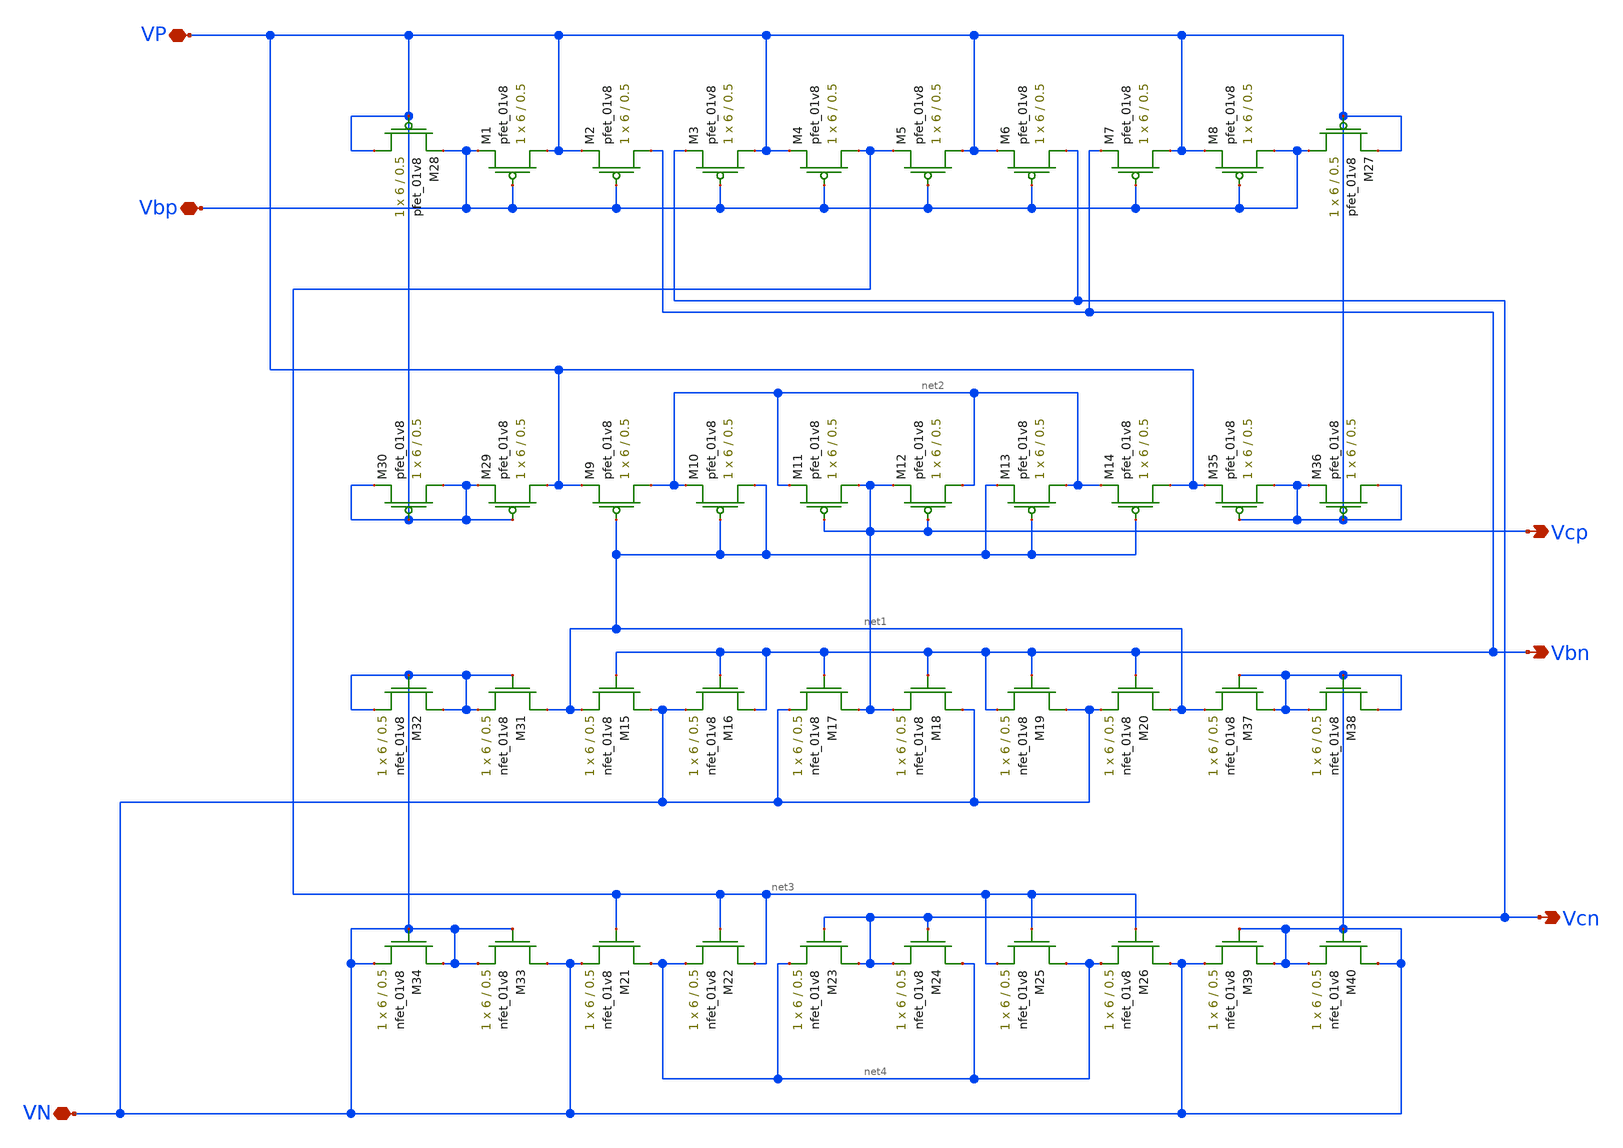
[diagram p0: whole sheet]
** sch_path: MP3/bias-lds.sch
**.subckt bias-lds VP VN Vbp Vcp VN Vbn Vcn
*.iopin VP
*.iopin VN
*.iopin Vbp
*.opin Vcp
*.iopin VN
*.opin Vbn
*.opin Vcn
XM1 VP Vbp Vbp VDD sky130_fd_pr__pfet_01v8 L=0.5 W=6 nf=1 ad='int((nf+1)/2) * W/nf * 0.29' as='int((nf+2)/2) * W/nf * 0.29'
+ pd='2*int((nf+1)/2) * (W/nf + 0.29)' ps='2*int((nf+2)/2) * (W/nf + 0.29)' nrd='0.29 / W' nrs='0.29 / W'
+ sa=0 sb=0 sd=0 mult=1 m=1
XM2 Vbn Vbp VP VDD sky130_fd_pr__pfet_01v8 L=0.5 W=6 nf=1 ad='int((nf+1)/2) * W/nf * 0.29' as='int((nf+2)/2) * W/nf * 0.29'
+ pd='2*int((nf+1)/2) * (W/nf + 0.29)' ps='2*int((nf+2)/2) * (W/nf + 0.29)' nrd='0.29 / W' nrs='0.29 / W'
+ sa=0 sb=0 sd=0 mult=1 m=1
XM3 VP Vbp Vcn VDD sky130_fd_pr__pfet_01v8 L=0.5 W=6 nf=1 ad='int((nf+1)/2) * W/nf * 0.29' as='int((nf+2)/2) * W/nf * 0.29'
+ pd='2*int((nf+1)/2) * (W/nf + 0.29)' ps='2*int((nf+2)/2) * (W/nf + 0.29)' nrd='0.29 / W' nrs='0.29 / W'
+ sa=0 sb=0 sd=0 mult=1 m=1
XM4 net3 Vbp VP VDD sky130_fd_pr__pfet_01v8 L=0.5 W=6 nf=1 ad='int((nf+1)/2) * W/nf * 0.29' as='int((nf+2)/2) * W/nf * 0.29'
+ pd='2*int((nf+1)/2) * (W/nf + 0.29)' ps='2*int((nf+2)/2) * (W/nf + 0.29)' nrd='0.29 / W' nrs='0.29 / W'
+ sa=0 sb=0 sd=0 mult=1 m=1
XM5 VP Vbp net3 VDD sky130_fd_pr__pfet_01v8 L=0.5 W=6 nf=1 ad='int((nf+1)/2) * W/nf * 0.29' as='int((nf+2)/2) * W/nf * 0.29'
+ pd='2*int((nf+1)/2) * (W/nf + 0.29)' ps='2*int((nf+2)/2) * (W/nf + 0.29)' nrd='0.29 / W' nrs='0.29 / W'
+ sa=0 sb=0 sd=0 mult=1 m=1
XM6 Vcn Vbp VP VDD sky130_fd_pr__pfet_01v8 L=0.5 W=6 nf=1 ad='int((nf+1)/2) * W/nf * 0.29' as='int((nf+2)/2) * W/nf * 0.29'
+ pd='2*int((nf+1)/2) * (W/nf + 0.29)' ps='2*int((nf+2)/2) * (W/nf + 0.29)' nrd='0.29 / W' nrs='0.29 / W'
+ sa=0 sb=0 sd=0 mult=1 m=1
XM7 VP Vbp Vbn VDD sky130_fd_pr__pfet_01v8 L=0.5 W=6 nf=1 ad='int((nf+1)/2) * W/nf * 0.29' as='int((nf+2)/2) * W/nf * 0.29'
+ pd='2*int((nf+1)/2) * (W/nf + 0.29)' ps='2*int((nf+2)/2) * (W/nf + 0.29)' nrd='0.29 / W' nrs='0.29 / W'
+ sa=0 sb=0 sd=0 mult=1 m=1
XM8 Vbp Vbp VP VDD sky130_fd_pr__pfet_01v8 L=0.5 W=6 nf=1 ad='int((nf+1)/2) * W/nf * 0.29' as='int((nf+2)/2) * W/nf * 0.29'
+ pd='2*int((nf+1)/2) * (W/nf + 0.29)' ps='2*int((nf+2)/2) * (W/nf + 0.29)' nrd='0.29 / W' nrs='0.29 / W'
+ sa=0 sb=0 sd=0 mult=1 m=1
XM9 net2 net1 VP VDD sky130_fd_pr__pfet_01v8 L=0.5 W=6 nf=1 ad='int((nf+1)/2) * W/nf * 0.29' as='int((nf+2)/2) * W/nf * 0.29'
+ pd='2*int((nf+1)/2) * (W/nf + 0.29)' ps='2*int((nf+2)/2) * (W/nf + 0.29)' nrd='0.29 / W' nrs='0.29 / W'
+ sa=0 sb=0 sd=0 mult=1 m=1
XM10 net1 net1 net2 VDD sky130_fd_pr__pfet_01v8 L=0.5 W=6 nf=1 ad='int((nf+1)/2) * W/nf * 0.29' as='int((nf+2)/2) * W/nf * 0.29'
+ pd='2*int((nf+1)/2) * (W/nf + 0.29)' ps='2*int((nf+2)/2) * (W/nf + 0.29)' nrd='0.29 / W' nrs='0.29 / W'
+ sa=0 sb=0 sd=0 mult=1 m=1
XM11 Vcp Vcp net2 VDD sky130_fd_pr__pfet_01v8 L=0.5 W=6 nf=1 ad='int((nf+1)/2) * W/nf * 0.29' as='int((nf+2)/2) * W/nf * 0.29'
+ pd='2*int((nf+1)/2) * (W/nf + 0.29)' ps='2*int((nf+2)/2) * (W/nf + 0.29)' nrd='0.29 / W' nrs='0.29 / W'
+ sa=0 sb=0 sd=0 mult=1 m=1
XM12 net2 Vcp Vcp VDD sky130_fd_pr__pfet_01v8 L=0.5 W=6 nf=1 ad='int((nf+1)/2) * W/nf * 0.29' as='int((nf+2)/2) * W/nf * 0.29'
+ pd='2*int((nf+1)/2) * (W/nf + 0.29)' ps='2*int((nf+2)/2) * (W/nf + 0.29)' nrd='0.29 / W' nrs='0.29 / W'
+ sa=0 sb=0 sd=0 mult=1 m=1
XM13 net2 net1 net1 VDD sky130_fd_pr__pfet_01v8 L=0.5 W=6 nf=1 ad='int((nf+1)/2) * W/nf * 0.29' as='int((nf+2)/2) * W/nf * 0.29'
+ pd='2*int((nf+1)/2) * (W/nf + 0.29)' ps='2*int((nf+2)/2) * (W/nf + 0.29)' nrd='0.29 / W' nrs='0.29 / W'
+ sa=0 sb=0 sd=0 mult=1 m=1
XM14 VP net1 net2 VDD sky130_fd_pr__pfet_01v8 L=0.5 W=6 nf=1 ad='int((nf+1)/2) * W/nf * 0.29' as='int((nf+2)/2) * W/nf * 0.29'
+ pd='2*int((nf+1)/2) * (W/nf + 0.29)' ps='2*int((nf+2)/2) * (W/nf + 0.29)' nrd='0.29 / W' nrs='0.29 / W'
+ sa=0 sb=0 sd=0 mult=1 m=1
XM15 VN Vbn net1 GND sky130_fd_pr__nfet_01v8 L=0.5 W=6 nf=1 ad='int((nf+1)/2) * W/nf * 0.29' as='int((nf+2)/2) * W/nf * 0.29'
+ pd='2*int((nf+1)/2) * (W/nf + 0.29)' ps='2*int((nf+2)/2) * (W/nf + 0.29)' nrd='0.29 / W' nrs='0.29 / W'
+ sa=0 sb=0 sd=0 mult=1 m=1
XM16 Vbn Vbn VN GND sky130_fd_pr__nfet_01v8 L=0.5 W=6 nf=1 ad='int((nf+1)/2) * W/nf * 0.29' as='int((nf+2)/2) * W/nf * 0.29'
+ pd='2*int((nf+1)/2) * (W/nf + 0.29)' ps='2*int((nf+2)/2) * (W/nf + 0.29)' nrd='0.29 / W' nrs='0.29 / W'
+ sa=0 sb=0 sd=0 mult=1 m=1
XM17 Vcp Vbn VN GND sky130_fd_pr__nfet_01v8 L=0.5 W=6 nf=1 ad='int((nf+1)/2) * W/nf * 0.29' as='int((nf+2)/2) * W/nf * 0.29'
+ pd='2*int((nf+1)/2) * (W/nf + 0.29)' ps='2*int((nf+2)/2) * (W/nf + 0.29)' nrd='0.29 / W' nrs='0.29 / W'
+ sa=0 sb=0 sd=0 mult=1 m=1
XM18 VN Vbn Vcp GND sky130_fd_pr__nfet_01v8 L=0.5 W=6 nf=1 ad='int((nf+1)/2) * W/nf * 0.29' as='int((nf+2)/2) * W/nf * 0.29'
+ pd='2*int((nf+1)/2) * (W/nf + 0.29)' ps='2*int((nf+2)/2) * (W/nf + 0.29)' nrd='0.29 / W' nrs='0.29 / W'
+ sa=0 sb=0 sd=0 mult=1 m=1
XM19 VN Vbn Vbn GND sky130_fd_pr__nfet_01v8 L=0.5 W=6 nf=1 ad='int((nf+1)/2) * W/nf * 0.29' as='int((nf+2)/2) * W/nf * 0.29'
+ pd='2*int((nf+1)/2) * (W/nf + 0.29)' ps='2*int((nf+2)/2) * (W/nf + 0.29)' nrd='0.29 / W' nrs='0.29 / W'
+ sa=0 sb=0 sd=0 mult=1 m=1
XM20 net1 Vbn VN GND sky130_fd_pr__nfet_01v8 L=0.5 W=6 nf=1 ad='int((nf+1)/2) * W/nf * 0.29' as='int((nf+2)/2) * W/nf * 0.29'
+ pd='2*int((nf+1)/2) * (W/nf + 0.29)' ps='2*int((nf+2)/2) * (W/nf + 0.29)' nrd='0.29 / W' nrs='0.29 / W'
+ sa=0 sb=0 sd=0 mult=1 m=1
XM21 net4 net3 VN GND sky130_fd_pr__nfet_01v8 L=0.5 W=6 nf=1 ad='int((nf+1)/2) * W/nf * 0.29' as='int((nf+2)/2) * W/nf * 0.29'
+ pd='2*int((nf+1)/2) * (W/nf + 0.29)' ps='2*int((nf+2)/2) * (W/nf + 0.29)' nrd='0.29 / W' nrs='0.29 / W'
+ sa=0 sb=0 sd=0 mult=1 m=1
XM22 net3 net3 net4 GND sky130_fd_pr__nfet_01v8 L=0.5 W=6 nf=1 ad='int((nf+1)/2) * W/nf * 0.29' as='int((nf+2)/2) * W/nf * 0.29'
+ pd='2*int((nf+1)/2) * (W/nf + 0.29)' ps='2*int((nf+2)/2) * (W/nf + 0.29)' nrd='0.29 / W' nrs='0.29 / W'
+ sa=0 sb=0 sd=0 mult=1 m=1
XM23 Vcn Vcn net4 GND sky130_fd_pr__nfet_01v8 L=0.5 W=6 nf=1 ad='int((nf+1)/2) * W/nf * 0.29' as='int((nf+2)/2) * W/nf * 0.29'
+ pd='2*int((nf+1)/2) * (W/nf + 0.29)' ps='2*int((nf+2)/2) * (W/nf + 0.29)' nrd='0.29 / W' nrs='0.29 / W'
+ sa=0 sb=0 sd=0 mult=1 m=1
XM24 net4 Vcn Vcn GND sky130_fd_pr__nfet_01v8 L=0.5 W=6 nf=1 ad='int((nf+1)/2) * W/nf * 0.29' as='int((nf+2)/2) * W/nf * 0.29'
+ pd='2*int((nf+1)/2) * (W/nf + 0.29)' ps='2*int((nf+2)/2) * (W/nf + 0.29)' nrd='0.29 / W' nrs='0.29 / W'
+ sa=0 sb=0 sd=0 mult=1 m=1
XM25 net4 net3 net3 GND sky130_fd_pr__nfet_01v8 L=0.5 W=6 nf=1 ad='int((nf+1)/2) * W/nf * 0.29' as='int((nf+2)/2) * W/nf * 0.29'
+ pd='2*int((nf+1)/2) * (W/nf + 0.29)' ps='2*int((nf+2)/2) * (W/nf + 0.29)' nrd='0.29 / W' nrs='0.29 / W'
+ sa=0 sb=0 sd=0 mult=1 m=1
XM26 VN net3 net4 GND sky130_fd_pr__nfet_01v8 L=0.5 W=6 nf=1 ad='int((nf+1)/2) * W/nf * 0.29' as='int((nf+2)/2) * W/nf * 0.29'
+ pd='2*int((nf+1)/2) * (W/nf + 0.29)' ps='2*int((nf+2)/2) * (W/nf + 0.29)' nrd='0.29 / W' nrs='0.29 / W'
+ sa=0 sb=0 sd=0 mult=1 m=1
XM27 Vbp VP VP VDD sky130_fd_pr__pfet_01v8 L=0.5 W=6 nf=1 ad='int((nf+1)/2) * W/nf * 0.29' as='int((nf+2)/2) * W/nf * 0.29'
+ pd='2*int((nf+1)/2) * (W/nf + 0.29)' ps='2*int((nf+2)/2) * (W/nf + 0.29)' nrd='0.29 / W' nrs='0.29 / W'
+ sa=0 sb=0 sd=0 mult=1 m=1
XM28 VP VP Vbp VDD sky130_fd_pr__pfet_01v8 L=0.5 W=6 nf=1 ad='int((nf+1)/2) * W/nf * 0.29' as='int((nf+2)/2) * W/nf * 0.29'
+ pd='2*int((nf+1)/2) * (W/nf + 0.29)' ps='2*int((nf+2)/2) * (W/nf + 0.29)' nrd='0.29 / W' nrs='0.29 / W'
+ sa=0 sb=0 sd=0 mult=1 m=1
XM29 VP VP VP VDD sky130_fd_pr__pfet_01v8 L=0.5 W=6 nf=1 ad='int((nf+1)/2) * W/nf * 0.29' as='int((nf+2)/2) * W/nf * 0.29'
+ pd='2*int((nf+1)/2) * (W/nf + 0.29)' ps='2*int((nf+2)/2) * (W/nf + 0.29)' nrd='0.29 / W' nrs='0.29 / W'
+ sa=0 sb=0 sd=0 mult=1 m=1
XM30 VP VP VP VDD sky130_fd_pr__pfet_01v8 L=0.5 W=6 nf=1 ad='int((nf+1)/2) * W/nf * 0.29' as='int((nf+2)/2) * W/nf * 0.29'
+ pd='2*int((nf+1)/2) * (W/nf + 0.29)' ps='2*int((nf+2)/2) * (W/nf + 0.29)' nrd='0.29 / W' nrs='0.29 / W'
+ sa=0 sb=0 sd=0 mult=1 m=1
XM31 net1 VN VN GND sky130_fd_pr__nfet_01v8 L=0.5 W=6 nf=1 ad='int((nf+1)/2) * W/nf * 0.29' as='int((nf+2)/2) * W/nf * 0.29'
+ pd='2*int((nf+1)/2) * (W/nf + 0.29)' ps='2*int((nf+2)/2) * (W/nf + 0.29)' nrd='0.29 / W' nrs='0.29 / W'
+ sa=0 sb=0 sd=0 mult=1 m=1
XM32 VN VN VN GND sky130_fd_pr__nfet_01v8 L=0.5 W=6 nf=1 ad='int((nf+1)/2) * W/nf * 0.29' as='int((nf+2)/2) * W/nf * 0.29'
+ pd='2*int((nf+1)/2) * (W/nf + 0.29)' ps='2*int((nf+2)/2) * (W/nf + 0.29)' nrd='0.29 / W' nrs='0.29 / W'
+ sa=0 sb=0 sd=0 mult=1 m=1
XM33 VN VN VN GND sky130_fd_pr__nfet_01v8 L=0.5 W=6 nf=1 ad='int((nf+1)/2) * W/nf * 0.29' as='int((nf+2)/2) * W/nf * 0.29'
+ pd='2*int((nf+1)/2) * (W/nf + 0.29)' ps='2*int((nf+2)/2) * (W/nf + 0.29)' nrd='0.29 / W' nrs='0.29 / W'
+ sa=0 sb=0 sd=0 mult=1 m=1
XM34 VN VN VN GND sky130_fd_pr__nfet_01v8 L=0.5 W=6 nf=1 ad='int((nf+1)/2) * W/nf * 0.29' as='int((nf+2)/2) * W/nf * 0.29'
+ pd='2*int((nf+1)/2) * (W/nf + 0.29)' ps='2*int((nf+2)/2) * (W/nf + 0.29)' nrd='0.29 / W' nrs='0.29 / W'
+ sa=0 sb=0 sd=0 mult=1 m=1
XM35 VP VP VP VDD sky130_fd_pr__pfet_01v8 L=0.5 W=6 nf=1 ad='int((nf+1)/2) * W/nf * 0.29' as='int((nf+2)/2) * W/nf * 0.29'
+ pd='2*int((nf+1)/2) * (W/nf + 0.29)' ps='2*int((nf+2)/2) * (W/nf + 0.29)' nrd='0.29 / W' nrs='0.29 / W'
+ sa=0 sb=0 sd=0 mult=1 m=1
XM36 VP VP VP VDD sky130_fd_pr__pfet_01v8 L=0.5 W=6 nf=1 ad='int((nf+1)/2) * W/nf * 0.29' as='int((nf+2)/2) * W/nf * 0.29'
+ pd='2*int((nf+1)/2) * (W/nf + 0.29)' ps='2*int((nf+2)/2) * (W/nf + 0.29)' nrd='0.29 / W' nrs='0.29 / W'
+ sa=0 sb=0 sd=0 mult=1 m=1
XM37 VN VN net1 GND sky130_fd_pr__nfet_01v8 L=0.5 W=6 nf=1 ad='int((nf+1)/2) * W/nf * 0.29' as='int((nf+2)/2) * W/nf * 0.29'
+ pd='2*int((nf+1)/2) * (W/nf + 0.29)' ps='2*int((nf+2)/2) * (W/nf + 0.29)' nrd='0.29 / W' nrs='0.29 / W'
+ sa=0 sb=0 sd=0 mult=1 m=1
XM38 VN VN VN GND sky130_fd_pr__nfet_01v8 L=0.5 W=6 nf=1 ad='int((nf+1)/2) * W/nf * 0.29' as='int((nf+2)/2) * W/nf * 0.29'
+ pd='2*int((nf+1)/2) * (W/nf + 0.29)' ps='2*int((nf+2)/2) * (W/nf + 0.29)' nrd='0.29 / W' nrs='0.29 / W'
+ sa=0 sb=0 sd=0 mult=1 m=1
XM39 VN VN VN GND sky130_fd_pr__nfet_01v8 L=0.5 W=6 nf=1 ad='int((nf+1)/2) * W/nf * 0.29' as='int((nf+2)/2) * W/nf * 0.29'
+ pd='2*int((nf+1)/2) * (W/nf + 0.29)' ps='2*int((nf+2)/2) * (W/nf + 0.29)' nrd='0.29 / W' nrs='0.29 / W'
+ sa=0 sb=0 sd=0 mult=1 m=1
XM40 VN VN VN GND sky130_fd_pr__nfet_01v8 L=0.5 W=6 nf=1 ad='int((nf+1)/2) * W/nf * 0.29' as='int((nf+2)/2) * W/nf * 0.29'
+ pd='2*int((nf+1)/2) * (W/nf + 0.29)' ps='2*int((nf+2)/2) * (W/nf + 0.29)' nrd='0.29 / W' nrs='0.29 / W'
+ sa=0 sb=0 sd=0 mult=1 m=1
**.ends
.end
